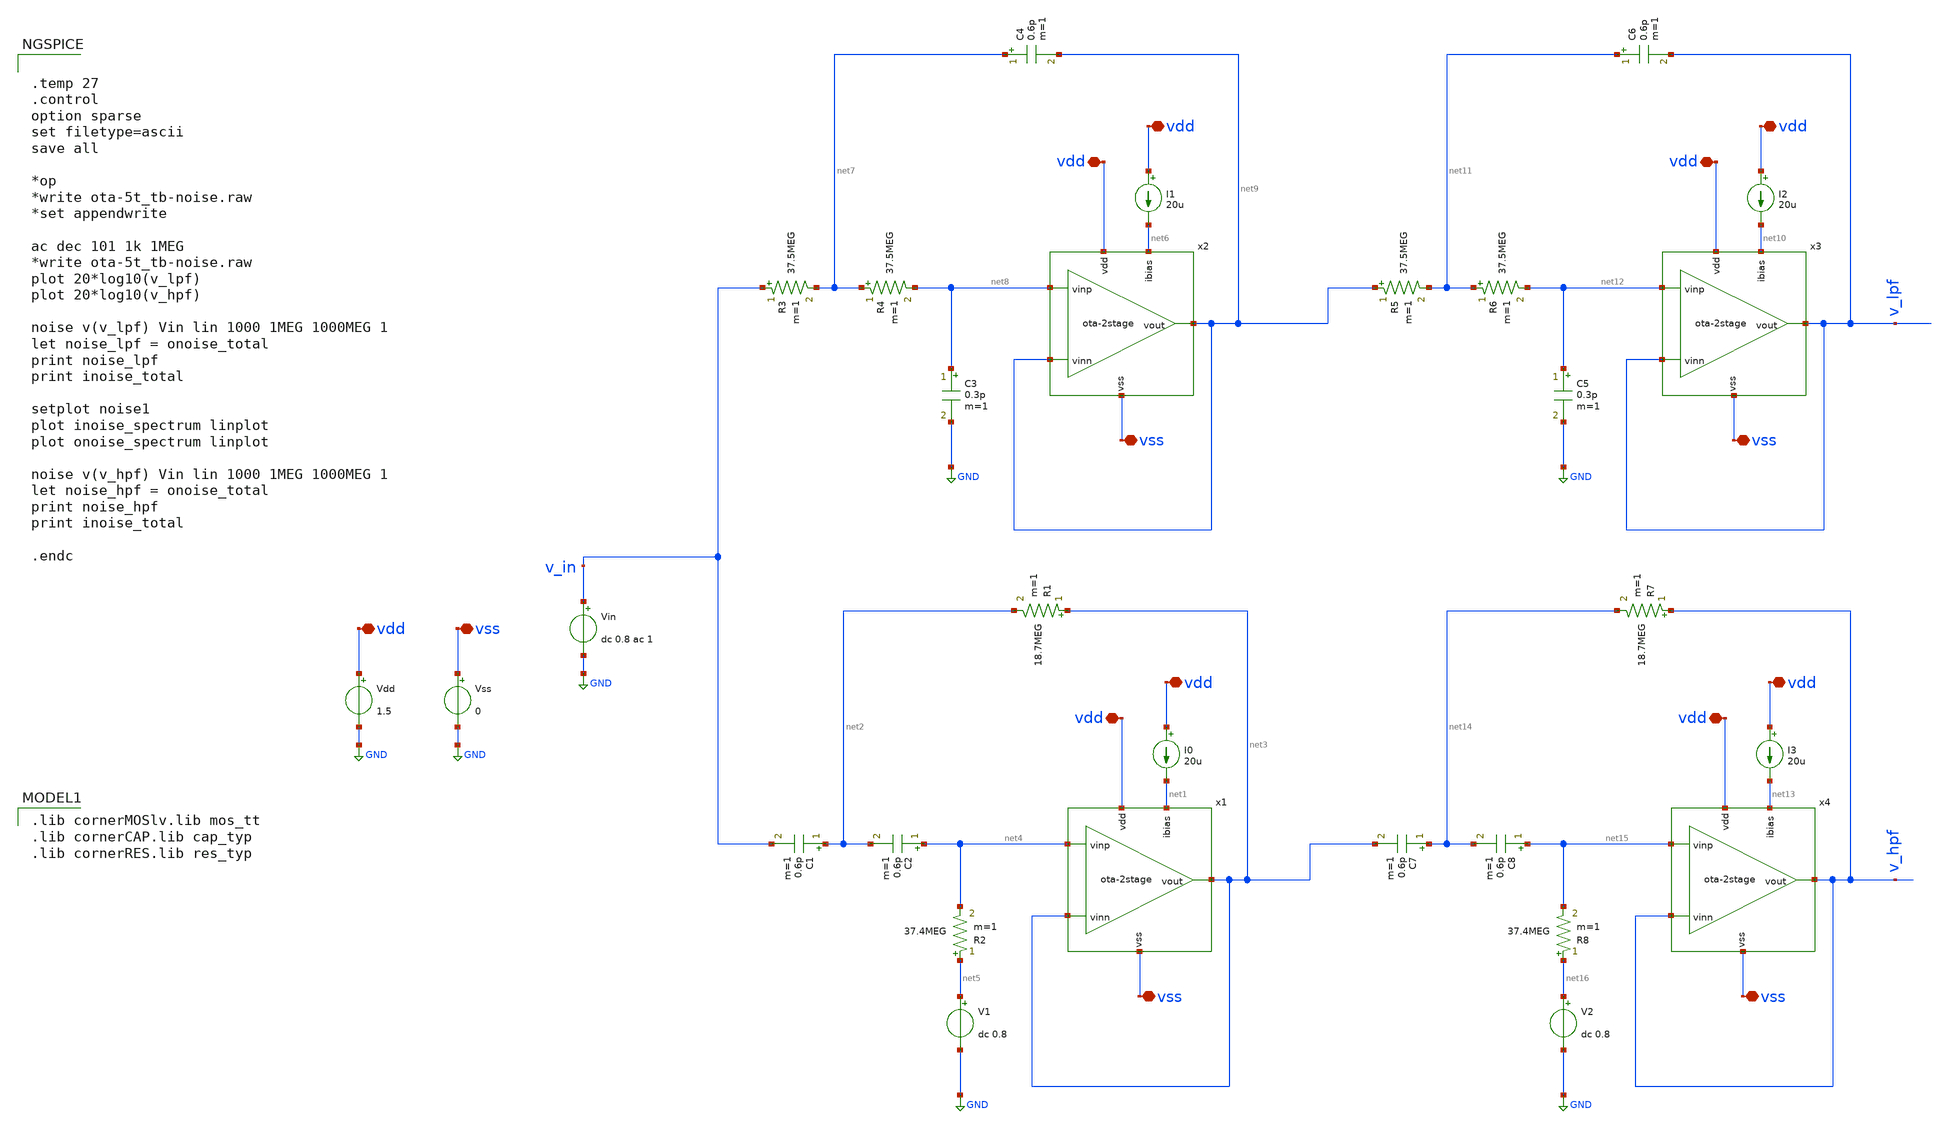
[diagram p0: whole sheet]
** sch_path: xschem/ota-2stage_tb-lr4-noise.sch
**.subckt ota-2stage_tb-lr4-noise vdd vdd vdd vss vss vdd vdd vss vdd vdd vss vdd vdd vss
*.iopin vdd
*.iopin vdd
*.iopin vdd
*.iopin vss
*.iopin vss
*.iopin vdd
*.iopin vdd
*.iopin vss
*.iopin vdd
*.iopin vdd
*.iopin vss
*.iopin vdd
*.iopin vdd
*.iopin vss
I0 vdd net1 20u
Vdd vdd GND 1.5
Vss vss GND 0
Vin v_in GND dc 0.8 ac 1
x1 vdd net1 net3 net3 net4 vss ota-2stage
R1 net3 net2 18.7MEG m=1
R2 net5 net4 37.4MEG m=1
C1 net2 v_in 0.6p m=1
C2 net4 net2 0.6p m=1
V1 net5 GND dc 0.8
I1 vdd net6 20u
R3 v_in net7 37.5MEG m=1
R4 net7 net8 37.5MEG m=1
C3 net8 GND 0.3p m=1
C4 net7 net9 0.6p m=1
x2 vdd net6 net9 net9 net8 vss ota-2stage
I2 vdd net10 20u
R5 net9 net11 37.5MEG m=1
R6 net11 net12 37.5MEG m=1
C5 net12 GND 0.3p m=1
C6 net11 v_lpf 0.6p m=1
x3 vdd net10 v_lpf v_lpf net12 vss ota-2stage
I3 vdd net13 20u
x4 vdd net13 v_hpf v_hpf net15 vss ota-2stage
R7 v_hpf net14 18.7MEG m=1
R8 net16 net15 37.4MEG m=1
C7 net14 net3 0.6p m=1
C8 net15 net14 0.6p m=1
V2 net16 GND dc 0.8
**** begin user architecture code
 .lib cornerMOSlv.lib mos_tt
.lib cornerCAP.lib cap_typ
.lib cornerRES.lib res_typ



.temp 27
.control
option sparse
set filetype=ascii
save all

*op
*write ota-5t_tb-noise.raw
*set appendwrite

ac dec 101 1k 1MEG
*write ota-5t_tb-noise.raw
plot 20*log10(v_lpf)
plot 20*log10(v_hpf)

noise v(v_lpf) Vin lin 1000 1MEG 1000MEG 1
let noise_lpf = onoise_total
print noise_lpf
print inoise_total

setplot noise1
plot inoise_spectrum linplot
plot onoise_spectrum linplot

noise v(v_hpf) Vin lin 1000 1MEG 1000MEG 1
let noise_hpf = onoise_total
print noise_hpf
print inoise_total

.endc


**** end user architecture code
**.ends
.GLOBAL GND
.end
